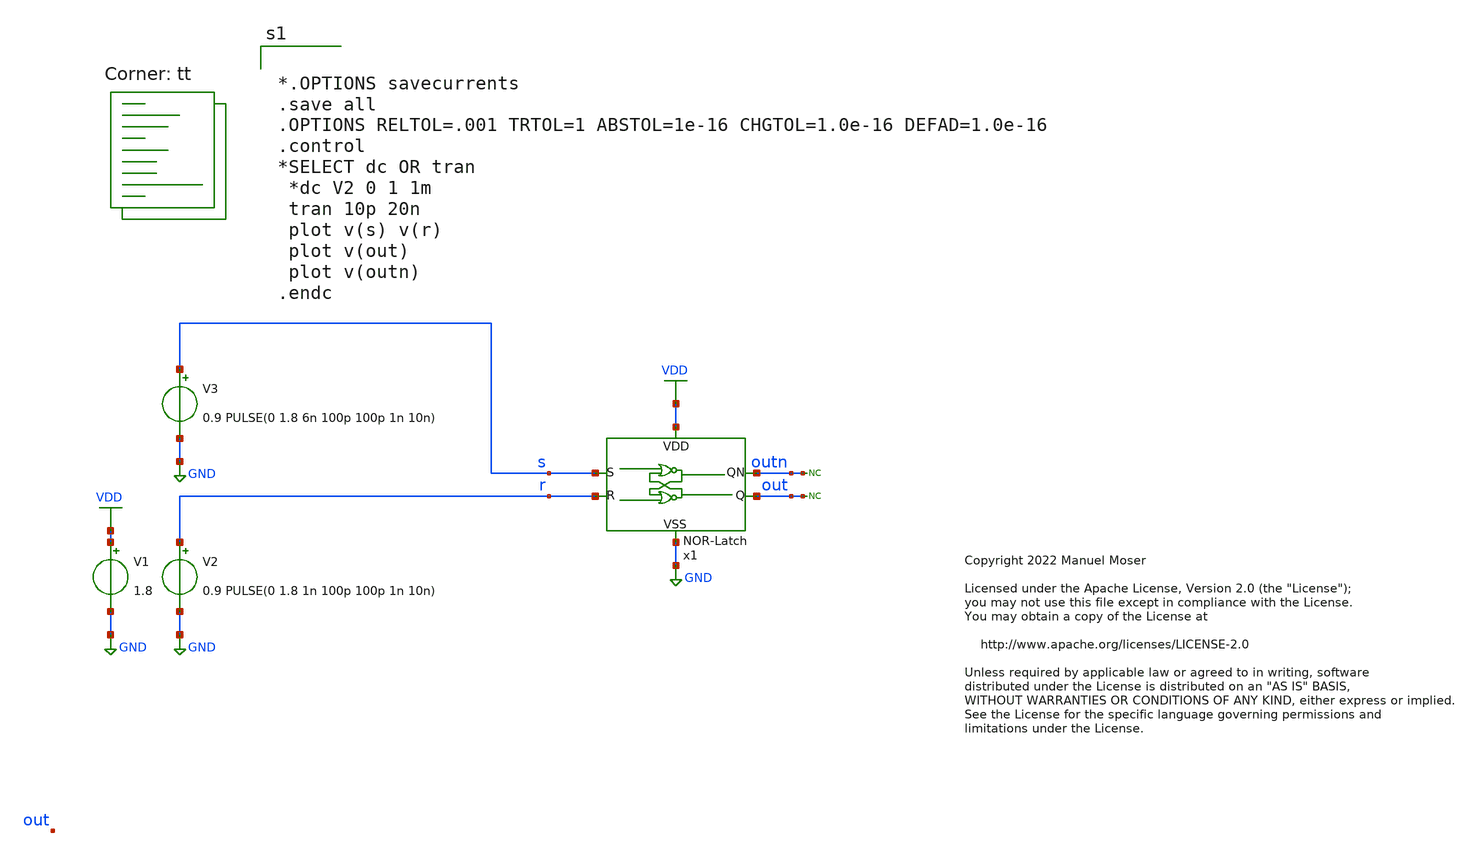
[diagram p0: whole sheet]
** sch_path: xschem/NOR-Latch/NOR-Latch_tb.sch
* Copyright 2022 Manuel Moser
* Licensed under the Apache License, Version 2.0 (the "License");
**.subckt NOR-Latch_tb
V1 VDD GND 1.8
V3 s GND 0.9 PULSE(0 1.8 6n 100p 100p 1n 10n)
V2 r GND 0.9 PULSE(0 1.8 1n 100p 100p 1n 10n)
* noconn out
x1 s outn VDD out GND r NOR-Latch
* noconn outn
**** begin user architecture code


*.OPTIONS savecurrents
.save all
.OPTIONS RELTOL=.001 TRTOL=1 ABSTOL=1e-16 CHGTOL=1.0e-16 DEFAD=1.0e-16
.control
*SELECT dc OR tran
 *dc V2 0 1 1m
 tran 10p 20n
 plot v(s) v(r)
 plot v(out)
 plot v(outn)
.endc


.lib $::SKYWATER_MODELS/sky130.lib.spice tt
**** end user architecture code
**.ends
.GLOBAL GND
.GLOBAL VDD
.end
